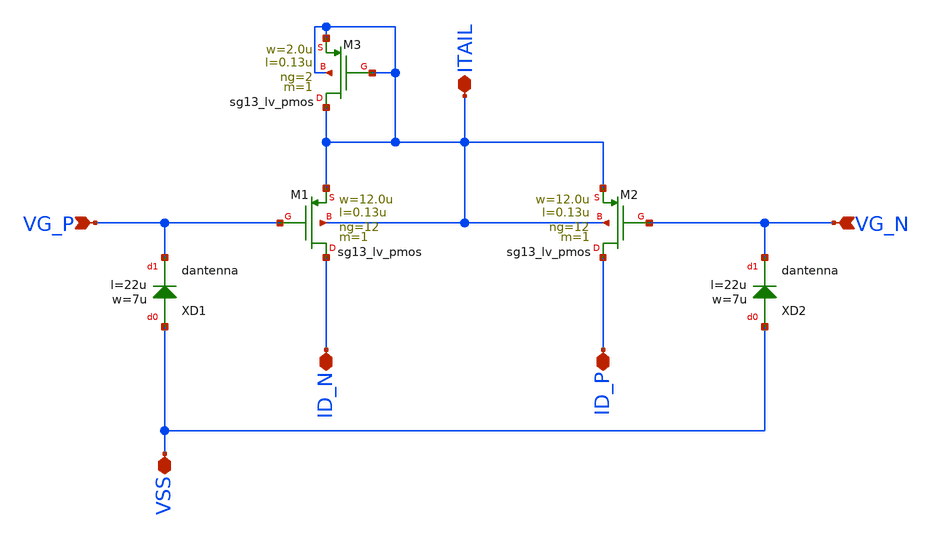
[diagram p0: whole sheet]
** sch_path: JKU_TC1/design_data/sfl-test-cells/xschem/diffpairs/dp_p_10u_130n.sch
**.subckt dp_p_10u_130n VG_P VG_N VSS ITAIL ID_N ID_P
*.ipin VG_P
*.ipin VG_N
*.iopin VSS
*.iopin ITAIL
*.iopin ID_N
*.iopin ID_P
XXD1 VSS VG_P dantenna l=22u w=7u
XXD2 VSS VG_N dantenna l=22u w=7u
XM1 ID_N VG_P ITAIL ITAIL sg13_lv_pmos w=12.0u l=0.13u ng=12 m=1 mm_ok=1
XM2 ID_P VG_N ITAIL ITAIL sg13_lv_pmos w=12.0u l=0.13u ng=12 m=1 mm_ok=1
XM3 ITAIL ITAIL ITAIL ITAIL sg13_lv_pmos w=2.0u l=0.13u ng=2 m=1 mm_ok=1
**.ends
.end
